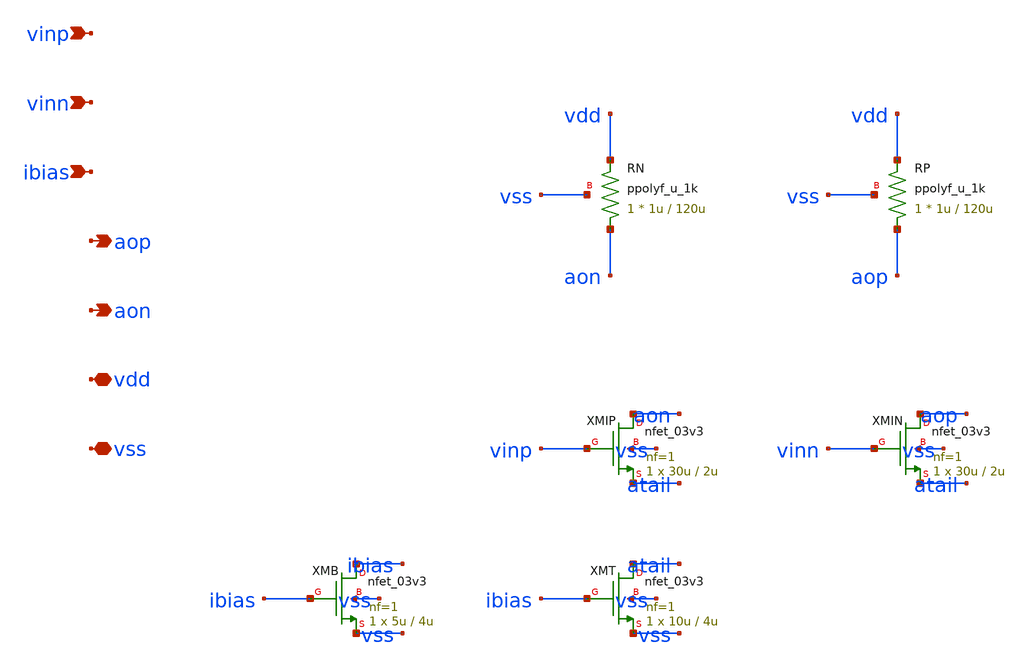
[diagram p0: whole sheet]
** sch_path: design/comparator_dut_analog.sch
**.subckt comparator_dut_analog vinp vinn ibias aop aon vdd vss
*.ipin vinp
*.ipin vinn
*.ipin ibias
*.opin aop
*.opin aon
*.iopin vdd
*.iopin vss
XMB ibias ibias vss vss nfet_03v3 L=4u W=5u nf=1 ad='int((nf+1)/2) * W/nf * 0.18u' as='int((nf+2)/2) * W/nf * 0.18u'
+ pd='2*int((nf+1)/2) * (W/nf + 0.18u)' ps='2*int((nf+2)/2) * (W/nf + 0.18u)' nrd='0.18u / W' nrs='0.18u / W'
+ sa=0 sb=0 sd=0 m=1
XMT atail ibias vss vss nfet_03v3 L=4u W=10u nf=1 ad='int((nf+1)/2) * W/nf * 0.18u' as='int((nf+2)/2) * W/nf * 0.18u'
+ pd='2*int((nf+1)/2) * (W/nf + 0.18u)' ps='2*int((nf+2)/2) * (W/nf + 0.18u)' nrd='0.18u / W' nrs='0.18u / W'
+ sa=0 sb=0 sd=0 m=1
XMIP aon vinp atail vss nfet_03v3 L=2u W=30u nf=1 ad='int((nf+1)/2) * W/nf * 0.18u' as='int((nf+2)/2) * W/nf * 0.18u'
+ pd='2*int((nf+1)/2) * (W/nf + 0.18u)' ps='2*int((nf+2)/2) * (W/nf + 0.18u)' nrd='0.18u / W' nrs='0.18u / W'
+ sa=0 sb=0 sd=0 m=1
XMIN aop vinn atail vss nfet_03v3 L=2u W=30u nf=1 ad='int((nf+1)/2) * W/nf * 0.18u' as='int((nf+2)/2) * W/nf * 0.18u'
+ pd='2*int((nf+1)/2) * (W/nf + 0.18u)' ps='2*int((nf+2)/2) * (W/nf + 0.18u)' nrd='0.18u / W' nrs='0.18u / W'
+ sa=0 sb=0 sd=0 m=1
XRN aon vdd vss ppolyf_u_1k r_width=1u r_length=120u m=1
XRP aop vdd vss ppolyf_u_1k r_width=1u r_length=120u m=1
**.ends
.end
